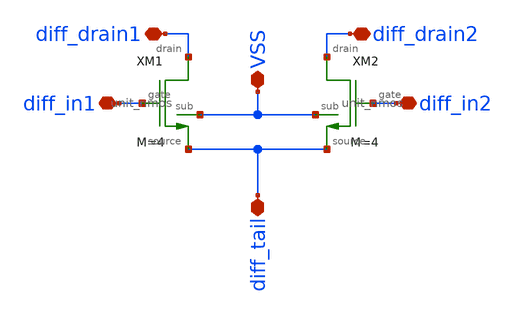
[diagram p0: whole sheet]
** sch_path: designs/libs/core_differential_pair/nmos_differential_pair/nmos_differential_pair.sch
**.subckt nmos_differential_pair diff_tail diff_in1 diff_in2 diff_drain1 diff_drain2 VSS
*.iopin diff_tail
*.iopin diff_in1
*.iopin diff_in2
*.iopin diff_drain1
*.iopin diff_drain2
*.iopin VSS
XM1 diff_drain1 VSS diff_in1 diff_tail unit_nmos M=4
XM2 diff_drain2 VSS diff_in2 diff_tail unit_nmos M=4
**.ends

* expanding   symbol:  libs/core_single_mos/unit_nmos/unit_nmos.sym # of pins=4
** sym_path: libs/core_single_mos/unit_nmos/unit_nmos.sym
** sch_path: libs/core_single_mos/unit_nmos/unit_nmos.sch
.subckt unit_nmos drain sub gate source
*.iopin drain
*.iopin source
*.iopin sub
*.iopin gate
XM1 drain gate source sub nfet_03v3 L=0.5u W=12u nf=2 ad='int((nf+1)/2) * W/nf * 0.18u' as='int((nf+2)/2) * W/nf * 0.18u'
+ pd='2*int((nf+1)/2) * (W/nf + 0.18u)' ps='2*int((nf+2)/2) * (W/nf + 0.18u)' nrd='0.18u / W' nrs='0.18u / W'
+ sa=0 sb=0 sd=0 m={M}
**** begin user architecture code

.param M=1

**** end user architecture code
.ends

.end
